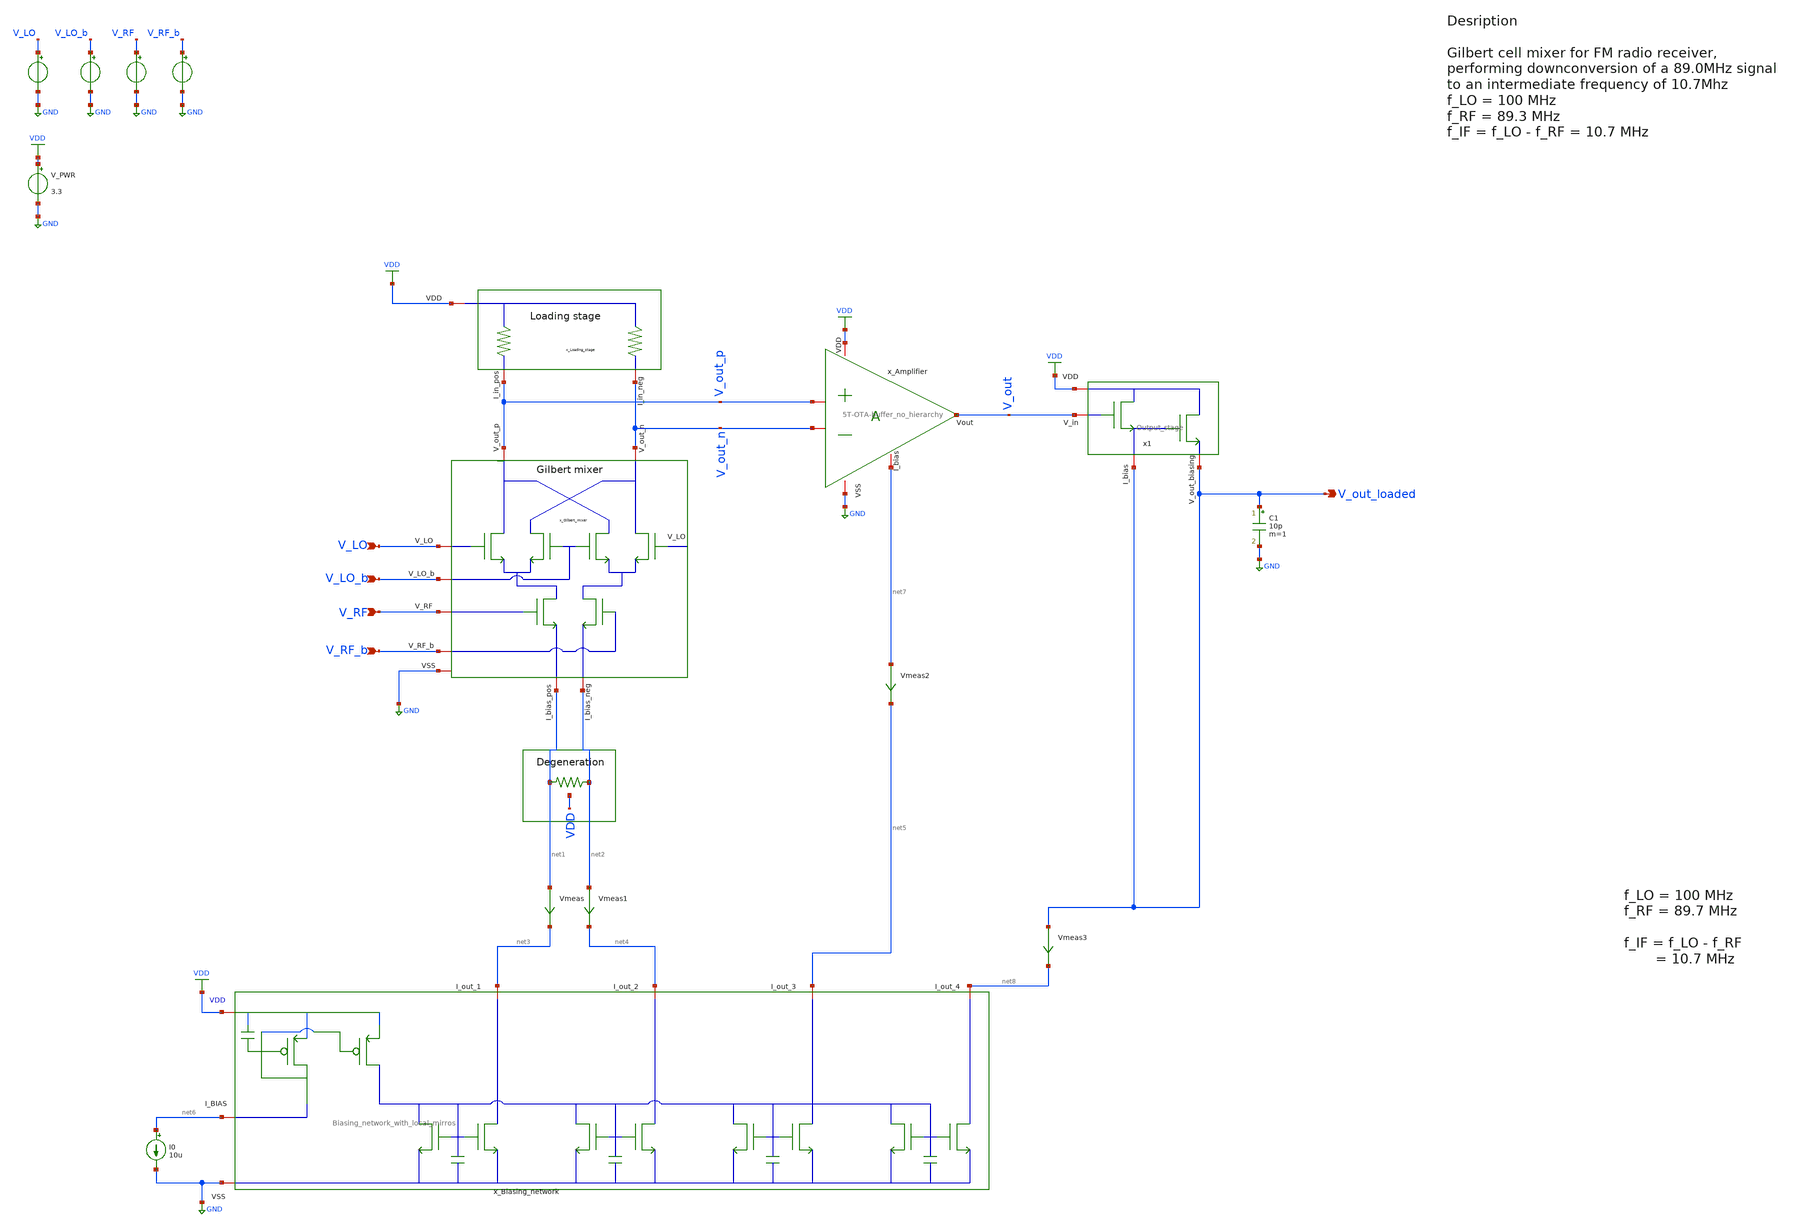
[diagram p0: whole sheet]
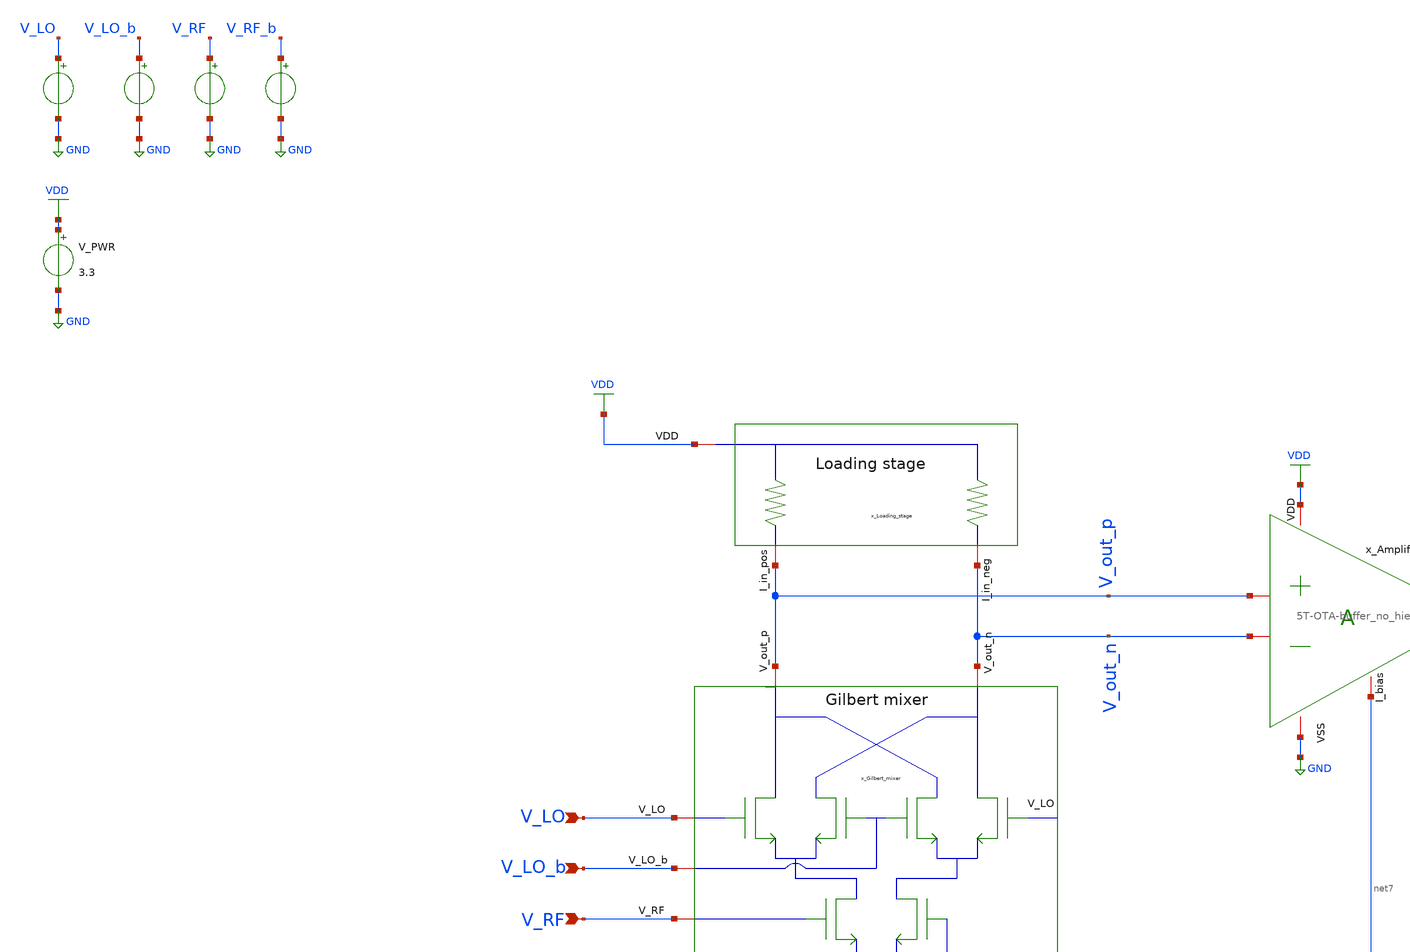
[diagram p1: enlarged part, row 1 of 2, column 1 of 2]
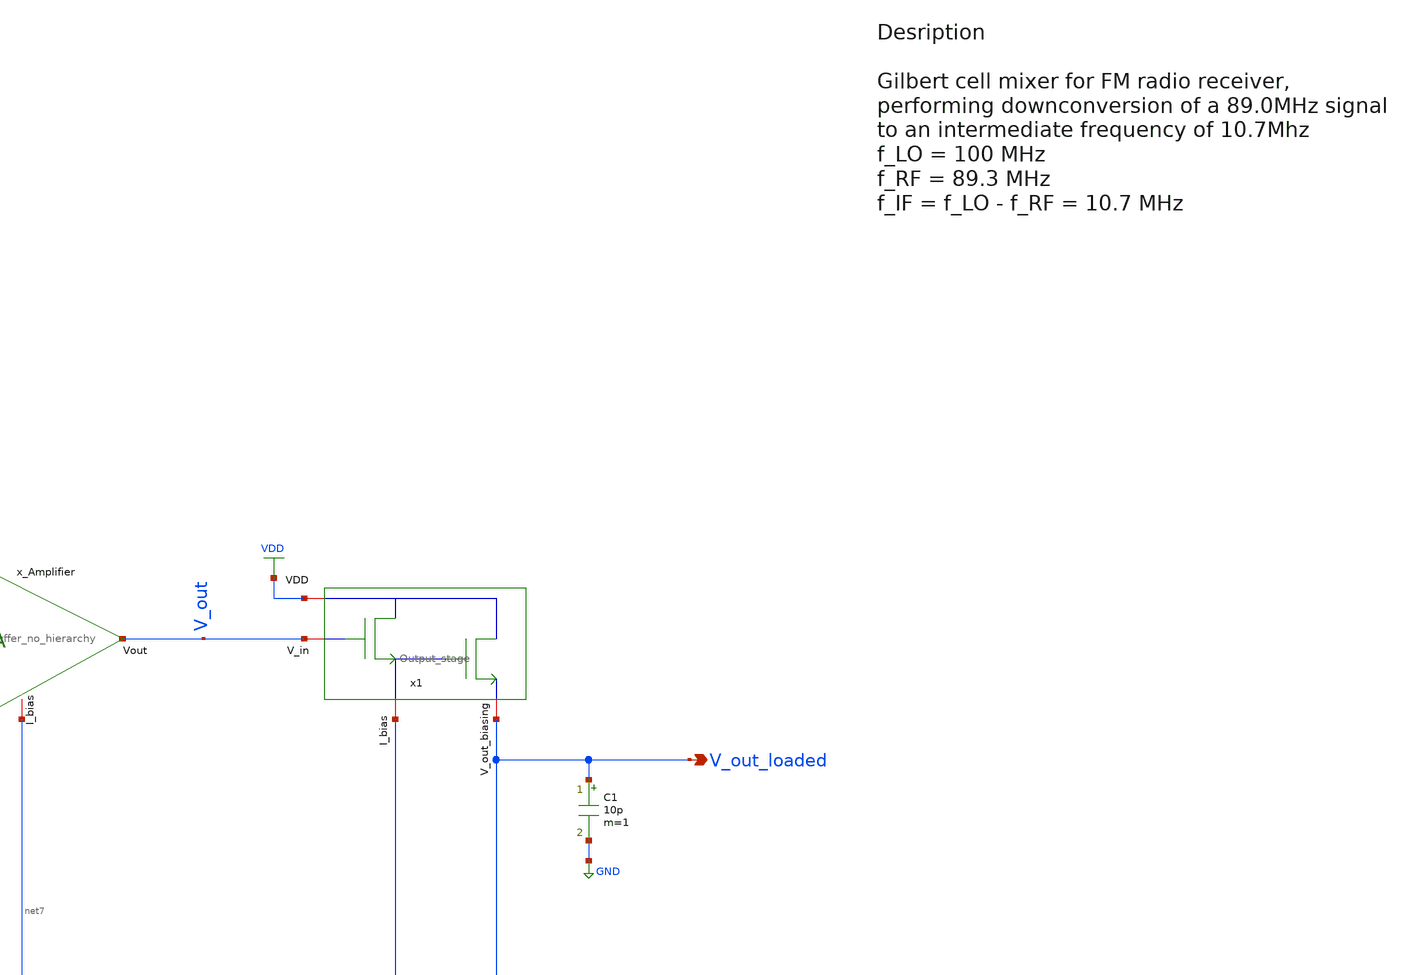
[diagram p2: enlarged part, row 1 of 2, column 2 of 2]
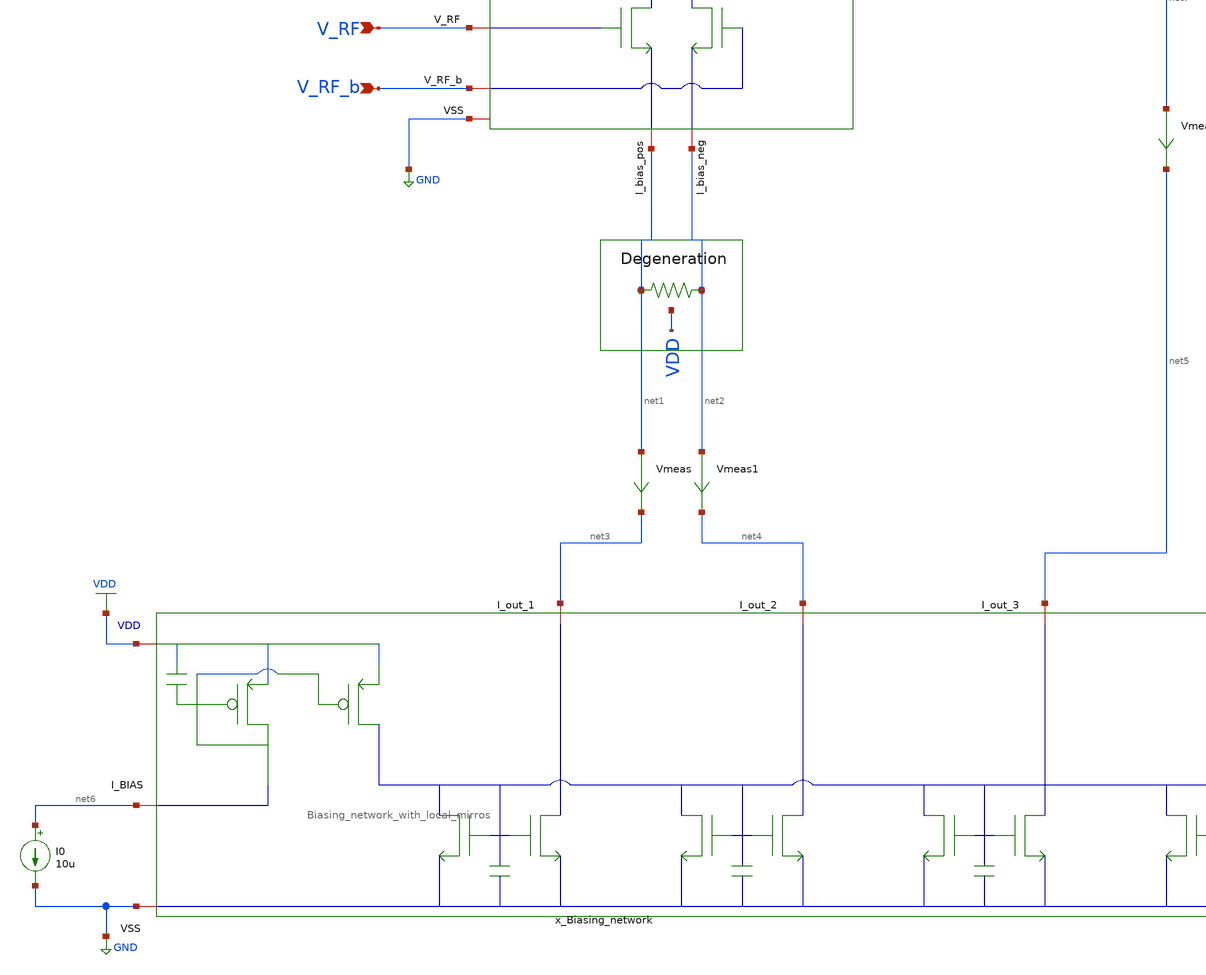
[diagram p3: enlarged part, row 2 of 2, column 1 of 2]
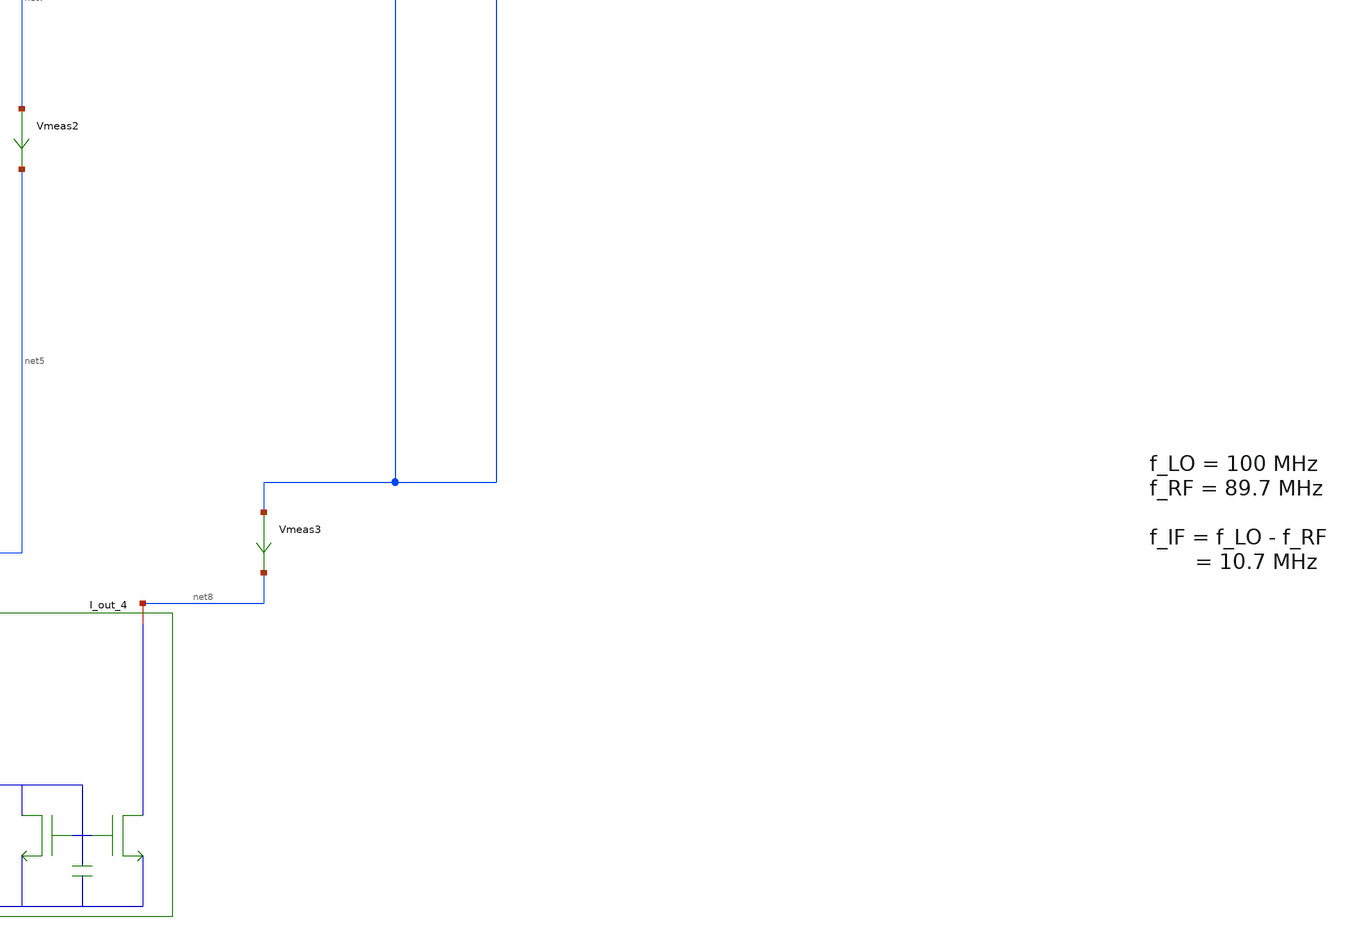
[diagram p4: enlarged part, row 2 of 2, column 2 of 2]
** sch_path: src/design_tb/PEX/Gilbert_cell_hierarchal_tb_PEX.sch
**.subckt Gilbert_cell_hierarchal_tb_PEX V_LO V_LO_b V_RF V_RF_b V_out_loaded
*.ipin V_LO
*.ipin V_LO_b
*.ipin V_RF
*.ipin V_RF_b
*.opin V_out_loaded
V_PWR VDD GND 3.3
.save i(v_pwr)
V_LO V_LO GND pulse(0 1.5 0 1p 1p 0.25n 0.5n)
.save i(v_lo)
V_LO_b V_LO_b GND pulse(0 1.5 0 1p 1p 0.25n 0.5n)
.save i(v_lo_b)
V_RF V_RF GND sin( 1 1 1 0 )
.save i(v_rf)
V_RF_b V_RF_b GND sin( 1 1 1 0 0 180 )
.save i(v_rf_b)
I0 net6 GND 10u
x_Loading_stage V_out_p V_out_n VDD Gilbert_cell_hierarchal_loading_stage
XR_load_3 net1 net2 VDD pplus_u r_width=0.5e-6 r_length=5e-6 m=1
x_Biasing_network VDD net3 net4 net5 net6 GND net8 Biasing_network_with_local_mirros pmos_l_ref=0.4u
+ pmos_w_ref=2u pmos_l_mir=0.4u pmos_w_mir=8u nmos_l_ref_1=1u nmos_w_ref_1=1.5u nmos_nf_ref_1=1 nmos_l_mir_1=1u
+ nmos_w_mir_1=7.5u nmos_nf_mir_1=5 nmos_l_ref_2=1u nmos_w_ref_2=1.5u nmos_nf_ref_2=1 nmos_l_mir_2=1u nmos_w_mir_2=7.5u
+ nmos_nf_mir_2=5 nmos_l_ref_3=1u nmos_w_ref_3=1.5u nmos_nf_ref_3=2 nmos_l_mir_3=1u nmos_w_mir_3=1.5u nmos_nf_mir_3=2
+ nmos_l_ref_4=1u nmos_w_ref_4=1.5u nmos_nf_ref_4=1 nmos_l_mir_4=1u nmos_w_mir_4=15u nmos_nf_mir_4=10
Vmeas net1 net3 0
.save i(vmeas)
Vmeas1 net2 net4 0
.save i(vmeas1)
x_Gilbert_mixer V_out_n V_out_p V_LO V_LO_b V_RF V_RF_b net1 net2 GND
+ Gilbert_cell_hierarchal_mixing_stage
x_Amplifier VDD V_out V_out_p V_out_n net7 GND 5T-OTA-buffer_no_hierarchy
Vmeas2 net7 net5 0
.save i(vmeas2)
x1 VDD V_out V_out_loaded V_out_loaded Output_stage
C1 V_out_loaded GND 10p m=1
Vmeas3 V_out_loaded net8 0
.save i(vmeas3)
**** begin user architecture code

.include $::180MCU_MODELS/design.ngspice
.include ~/Downloads/SSCS_PICO_2025/src/python/Gilbert_mixer_intedigited/lvs/netlists/Gilbert_mixer_extracted_layout_PEX.spice
.lib $::180MCU_MODELS/sm141064.ngspice typical
.lib $::180MCU_MODELS/sm141064.ngspice mimcap_typical
.lib $::180MCU_MODELS/sm141064.ngspice cap_mim
.lib $::180MCU_MODELS/sm141064.ngspice res_typical
.lib $::180MCU_MODELS/sm141064.ngspice diode_typical
.lib $::180MCU_MODELS/sm141064.ngspice bjt_typical
.lib $::180MCU_MODELS/sm141064.ngspice moscap_typical



.control

    * Set frequency and amplitude variables to proper values from within the control sequence
    * sine-wave LO
    * set cm_lo = 0.5
    * set freq_lo = 2.50G
    * set amp_lo = 0.5
    * alter @V_LO[sin] = [ $cm_lo $amp_lo $freq_lo 0 ]
    * alter @V_LO_b[sin] = [ $cm_lo $amp_lo $freq_lo 0 0 180 ]

    set freq_lo = 100Meg
    set cm_lo = 1.8
    set amp_lo = 0.4

    set cm_rf  = 1.2
    set freq_rf = 89.3Meg
    * set freq_rf = 10.7Meg
    set amp_rf  = 0.1

    * set the parameters to the voltage sources
    alter @V_LO[sin] = [ $cm_lo $amp_lo $freq_lo 0 ]
    alter @V_LO_b[sin] = [ $cm_lo $amp_lo $freq_lo 0 0 180 ]
    alter @V_RF[sin] = [ $cm_rf $amp_rf $freq_rf 0 ]
    alter @V_RF_b[sin] = [ $cm_rf $amp_rf $freq_rf 0 0 180 ]

    save all

    * operating point
    op
    show

    write Gilbert_cell_PEX.raw

    set appendwrite

    * Transient analysis to observe mixing operation
    tran 5p 0.5u
    write Gilbert_cell_PEX.raw

    * Calculate differential output for conversion gain measurement
    * let v_out_diff = v(v_out_p)-v(v_out_n)
    let v_out_diff = v(v_out)
    let v_rf_diff = v(v_rf)-v(v_rf_b)
    let v_lo_diff = v(v_lo)-v(v_lo_b)


    * Extract IF component at 100MHz using FFT
    linearize v_out_diff v_rf_diff v_lo_diff v_out_loaded
    let time_step = 1e-12
    let sample_freq = 1/time_step
    let npts = length(v_out_diff)
    let freq_res = sample_freq/npts


    fft v_out_diff v_rf_diff v_lo_diff v_out_loaded

    * print everything, sanity check
    * set     ; print all available global (?) variables (?)
    * setplot ; print all plots
    * display ; print variables available in current plot

    let freq_res = tran2.freq_res
    let freq_if = abs ( $freq_lo - $freq_rf )

    * Define bandwidth for power integration (10MHz around nominal frequencies).
    *  To improve resolution increase time of tran simulation, reduce time step, in order to reduce
+ FFT resolution
    let bandwidth = 15e6
    let bin_width = floor(bandwidth/freq_res + 0.5)
    print bin_width


    * Find center bins for RF and IF frequencies
    let rf_center_bin = floor( $freq_rf/freq_res + 0.5 )
    let if_center_bin = floor( freq_if/freq_res + 0.5 )
    print freq_if
    print freq_res
    print abs(v_out_diff[if_center_bin])
    print abs(v_out_diff[if_center_bin-1])
    print abs(v_out_diff[if_center_bin+1])



    * Calculate power by summing magnitude squared over the bandwidth
    * RF power integration (±10MHz around freq_rf)
    * let rf_power_total = 0
    * let i = rf_center_bin - bin_width
    * while i <= rf_center_bin + bin_width
    *     if i>0 & i < length(v_rf_diff)
    *         let bin_freq = i * freq_res
            * print bin_freq
            * print abs(v_rf_diff[i])
    *         let rf_power_total = rf_power_total + abs(v_rf_diff[i])^2
    *    end
    *     let i = i + 1
    * end
    set rf_power_total = $amp_rf * $amp_rf / 50

    * IF power integration (±10MHz around freq_if)
    let if_power_total = 0
    let j = if_center_bin - bin_width
    while j <= if_center_bin + bin_width
        if j >= 0 & j < length(v_out_diff)
            let bin_freq = j * freq_res
            print bin_freq
            print abs(v_out_diff[j])
            let if_power_total = if_power_total + abs(v_out_diff[j])^2
        end
        let j = j + 1
    end

    print if_power_total
    print rf_power_total

    let conversion_gain_db = 10*log10(if_power_total/rf_power_total)
    print conversion_gain_db

    write Gilbert_cell_PEX.raw

.endc


**** end user architecture code
**.ends
.GLOBAL VDD
.GLOBAL GND
.end
